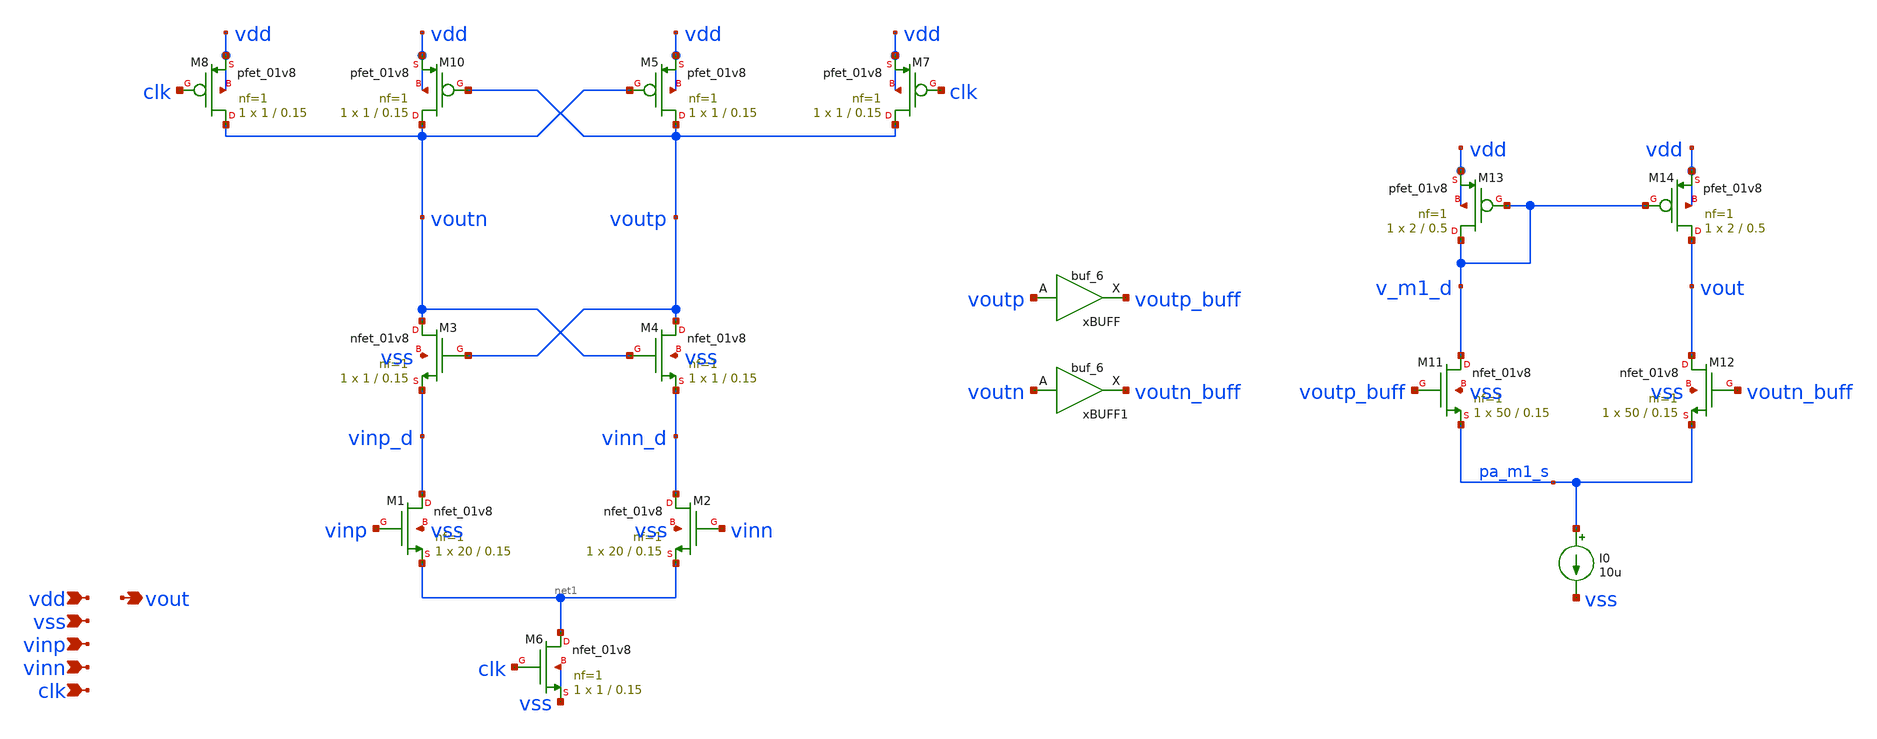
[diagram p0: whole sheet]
** sch_path: schematics/comp.sch
**.subckt comp vdd vout vss vinp vinn clk
*.ipin vdd
*.opin vout
*.ipin vss
*.ipin vinp
*.ipin vinn
*.ipin clk
XM6 net1 clk vss vss sky130_fd_pr__nfet_01v8 L=0.15 W=1 nf=1 ad='int((1 + 1)/2) * 1 / 1 * 0.29' as='int((1 + 2)/2) * 1 / 1 * 0.29'
+ pd='2*int((1 + 1)/2) * (1 / 1 + 0.29)' ps='2*int((1 + 2)/2) * (1 / 1 + 0.29)' nrd='0.29 / 1 ' nrs='0.29 / 1 '
+ sa=0 sb=0 sd=0 mult=1 m=1
XM10 voutn voutp vdd vdd sky130_fd_pr__pfet_01v8 L=0.15 W=1 nf=1 ad='int((1 + 1)/2) * 1 / 1 * 0.29' as='int((1 + 2)/2) * 1 / 1 * 0.29'
+ pd='2*int((1 + 1)/2) * (1 / 1 + 0.29)' ps='2*int((1 + 2)/2) * (1 / 1 + 0.29)' nrd='0.29 / 1 ' nrs='0.29 / 1 '
+ sa=0 sb=0 sd=0 mult=1 m=1
xBUFF voutp vss vss vdd vdd voutp_buff sky130_fd_sc_hd__buf_6
xBUFF1 voutn vss vss vdd vdd voutn_buff sky130_fd_sc_hd__buf_6
I0 pa_m1_s vss 10u
XM11 v_m1_d voutp_buff pa_m1_s vss sky130_fd_pr__nfet_01v8 L=0.15 W=50 nf=1 ad='int((1 + 1)/2) * 50 / 1 * 0.29'
+ as='int((1 + 2)/2) * 50 / 1 * 0.29' pd='2*int((1 + 1)/2) * (50 / 1 + 0.29)' ps='2*int((1 + 2)/2) * (50 / 1 + 0.29)'
+ nrd='0.29 / 50 ' nrs='0.29 / 50 ' sa=0 sb=0 sd=0 mult=1 m=1
XM12 vout voutn_buff pa_m1_s vss sky130_fd_pr__nfet_01v8 L=0.15 W=50 nf=1 ad='int((1 + 1)/2) * 50 / 1 * 0.29'
+ as='int((1 + 2)/2) * 50 / 1 * 0.29' pd='2*int((1 + 1)/2) * (50 / 1 + 0.29)' ps='2*int((1 + 2)/2) * (50 / 1 + 0.29)'
+ nrd='0.29 / 50 ' nrs='0.29 / 50 ' sa=0 sb=0 sd=0 mult=1 m=1
XM13 v_m1_d v_m1_d vdd vdd sky130_fd_pr__pfet_01v8 L=0.5 W=2 nf=1 ad='int((1 + 1)/2) * 2 / 1 * 0.29'
+ as='int((1 + 2)/2) * 2 / 1 * 0.29' pd='2*int((1 + 1)/2) * (2 / 1 + 0.29)' ps='2*int((1 + 2)/2) * (2 / 1 + 0.29)'
+ nrd='0.29 / 2 ' nrs='0.29 / 2 ' sa=0 sb=0 sd=0 mult=1 m=1
XM14 vout v_m1_d vdd vdd sky130_fd_pr__pfet_01v8 L=0.5 W=2 nf=1 ad='int((1 + 1)/2) * 2 / 1 * 0.29' as='int((1 + 2)/2) * 2 / 1 * 0.29'
+ pd='2*int((1 + 1)/2) * (2 / 1 + 0.29)' ps='2*int((1 + 2)/2) * (2 / 1 + 0.29)' nrd='0.29 / 2 ' nrs='0.29 / 2 '
+ sa=0 sb=0 sd=0 mult=1 m=1
XM1 vinp_d vinp net1 vss sky130_fd_pr__nfet_01v8 L=0.15 W=20 nf=1 ad='int((1 + 1)/2) * 20 / 1 * 0.29'
+ as='int((1 + 2)/2) * 20 / 1 * 0.29' pd='2*int((1 + 1)/2) * (20 / 1 + 0.29)' ps='2*int((1 + 2)/2) * (20 / 1 + 0.29)'
+ nrd='0.29 / 20 ' nrs='0.29 / 20 ' sa=0 sb=0 sd=0 mult=1 m=1
XM2 vinn_d vinn net1 vss sky130_fd_pr__nfet_01v8 L=0.15 W=20 nf=1 ad='int((1 + 1)/2) * 20 / 1 * 0.29'
+ as='int((1 + 2)/2) * 20 / 1 * 0.29' pd='2*int((1 + 1)/2) * (20 / 1 + 0.29)' ps='2*int((1 + 2)/2) * (20 / 1 + 0.29)'
+ nrd='0.29 / 20 ' nrs='0.29 / 20 ' sa=0 sb=0 sd=0 mult=1 m=1
XM3 voutn voutp vinp_d vss sky130_fd_pr__nfet_01v8 L=0.15 W=1 nf=1 ad='int((1 + 1)/2) * 1 / 1 * 0.29'
+ as='int((1 + 2)/2) * 1 / 1 * 0.29' pd='2*int((1 + 1)/2) * (1 / 1 + 0.29)' ps='2*int((1 + 2)/2) * (1 / 1 + 0.29)'
+ nrd='0.29 / 1 ' nrs='0.29 / 1 ' sa=0 sb=0 sd=0 mult=1 m=1
XM4 voutp voutn vinn_d vss sky130_fd_pr__nfet_01v8 L=0.15 W=1 nf=1 ad='int((1 + 1)/2) * 1 / 1 * 0.29'
+ as='int((1 + 2)/2) * 1 / 1 * 0.29' pd='2*int((1 + 1)/2) * (1 / 1 + 0.29)' ps='2*int((1 + 2)/2) * (1 / 1 + 0.29)'
+ nrd='0.29 / 1 ' nrs='0.29 / 1 ' sa=0 sb=0 sd=0 mult=1 m=1
XM5 voutp voutn vdd vdd sky130_fd_pr__pfet_01v8 L=0.15 W=1 nf=1 ad='int((1 + 1)/2) * 1 / 1 * 0.29' as='int((1 + 2)/2) * 1 / 1 * 0.29'
+ pd='2*int((1 + 1)/2) * (1 / 1 + 0.29)' ps='2*int((1 + 2)/2) * (1 / 1 + 0.29)' nrd='0.29 / 1 ' nrs='0.29 / 1 '
+ sa=0 sb=0 sd=0 mult=1 m=1
XM7 voutp clk vdd vdd sky130_fd_pr__pfet_01v8 L=0.15 W=1 nf=1 ad='int((1 + 1)/2) * 1 / 1 * 0.29' as='int((1 + 2)/2) * 1 / 1 * 0.29'
+ pd='2*int((1 + 1)/2) * (1 / 1 + 0.29)' ps='2*int((1 + 2)/2) * (1 / 1 + 0.29)' nrd='0.29 / 1 ' nrs='0.29 / 1 '
+ sa=0 sb=0 sd=0 mult=1 m=1
XM8 voutn clk vdd vdd sky130_fd_pr__pfet_01v8 L=0.15 W=1 nf=1 ad='int((1 + 1)/2) * 1 / 1 * 0.29' as='int((1 + 2)/2) * 1 / 1 * 0.29'
+ pd='2*int((1 + 1)/2) * (1 / 1 + 0.29)' ps='2*int((1 + 2)/2) * (1 / 1 + 0.29)' nrd='0.29 / 1 ' nrs='0.29 / 1 '
+ sa=0 sb=0 sd=0 mult=1 m=1
**.ends
.end
